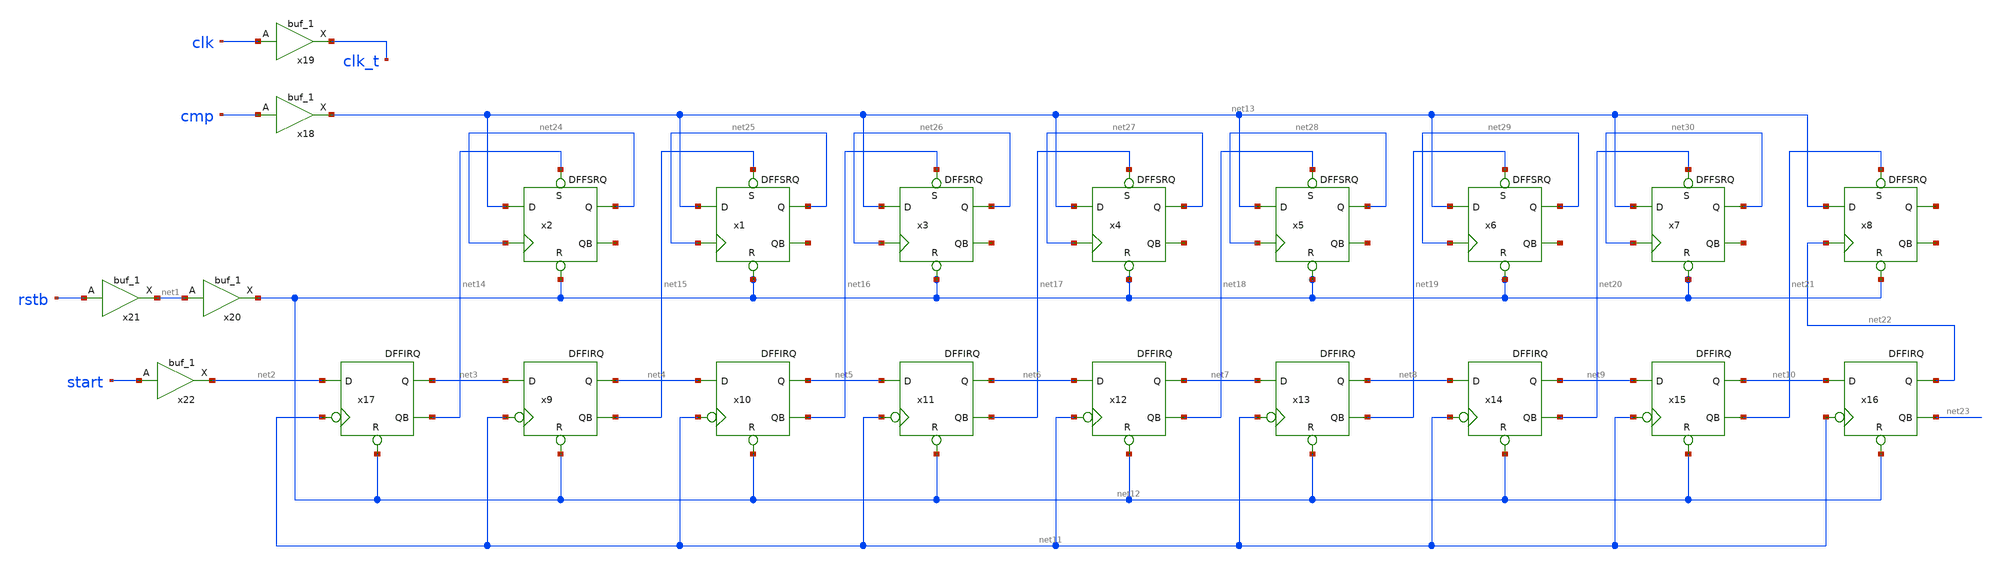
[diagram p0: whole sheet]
** sch_path: 8bitADC_SARLOGIC.sch
**.subckt 8bitADC_SARLOGIC
x2 net24 net31 net13 net24 net14 net12 VCC VSS VCC VSS DFFSRQ
x1 net25 net32 net13 net25 net15 net12 VCC VSS VCC VSS DFFSRQ
x3 net26 net33 net13 net26 net16 net12 VCC VSS VCC VSS DFFSRQ
x4 net27 net34 net13 net27 net17 net12 VCC VSS VCC VSS DFFSRQ
x5 net28 net35 net13 net28 net18 net12 VCC VSS VCC VSS DFFSRQ
x6 net29 net36 net13 net29 net19 net12 VCC VSS VCC VSS DFFSRQ
x7 net30 net37 net13 net30 net20 net12 VCC VSS VCC VSS DFFSRQ
x8 net38 net39 net13 net22 net21 net12 VCC VSS VCC VSS DFFSRQ
x9 net4 net15 net3 net11 net12 VCC VSS VCC VSS DFFIRQ
x10 net5 net16 net4 net11 net12 VCC VSS VCC VSS DFFIRQ
x11 net6 net17 net5 net11 net12 VCC VSS VCC VSS DFFIRQ
x12 net7 net18 net6 net11 net12 VCC VSS VCC VSS DFFIRQ
x13 net8 net19 net7 net11 net12 VCC VSS VCC VSS DFFIRQ
x14 net9 net20 net8 net11 net12 VCC VSS VCC VSS DFFIRQ
x15 net10 net21 net9 net11 net12 VCC VSS VCC VSS DFFIRQ
x16 net22 net23 net10 net11 net12 VCC VSS VCC VSS DFFIRQ
x17 net3 net14 net2 net11 net12 VCC VSS VCC VSS DFFIRQ
x18 cmp VSS VNB VPB VDD net13 sky130_fd_sc_hd__buf_1
x19 clk VSS VNB VPB VDD clk_t sky130_fd_sc_hd__buf_1
x20 net1 VSS VNB VPB VDD net12 sky130_fd_sc_hd__buf_1
x21 rstb VSS VNB VPB VDD net1 sky130_fd_sc_hd__buf_1
x22 start VSS VNB VPB VDD net2 sky130_fd_sc_hd__buf_1
**.ends
.end
